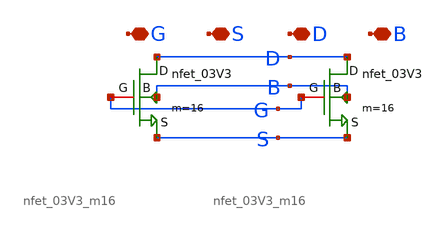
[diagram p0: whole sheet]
** sch_path: DAC_PAKISTAN_01/Pakistan1_Xschem/nfet_03V3_m32.sch
**.subckt nfet_03V3_m32 G S D B
*.iopin G
*.iopin S
*.iopin D
*.iopin B
x1 S D B G nfet_03V3_m16
x2 S D B G nfet_03V3_m16
**.ends
.end
